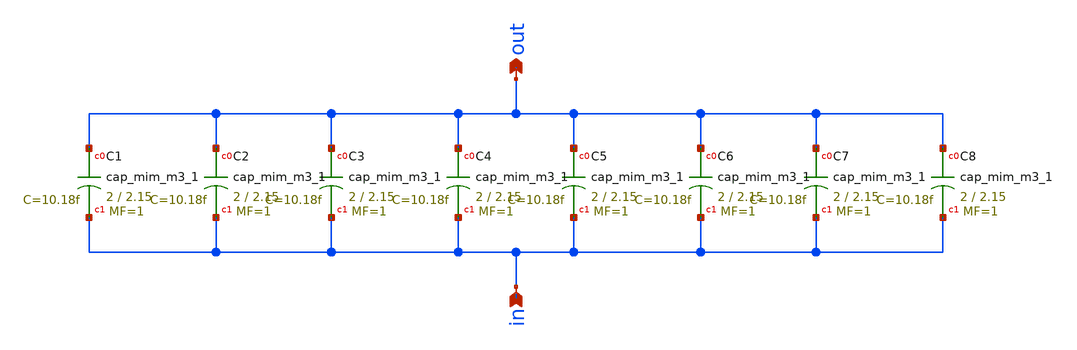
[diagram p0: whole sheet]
** sch_path: xschem/cap8.sch
**.subckt cap8 in out
*.ipin in
*.opin out
XC1 out in sky130_fd_pr__cap_mim_m3_1 W=2 L=2.15 MF=1 m=1
XC2 out in sky130_fd_pr__cap_mim_m3_1 W=2 L=2.15 MF=1 m=1
XC3 out in sky130_fd_pr__cap_mim_m3_1 W=2 L=2.15 MF=1 m=1
XC4 out in sky130_fd_pr__cap_mim_m3_1 W=2 L=2.15 MF=1 m=1
XC5 out in sky130_fd_pr__cap_mim_m3_1 W=2 L=2.15 MF=1 m=1
XC6 out in sky130_fd_pr__cap_mim_m3_1 W=2 L=2.15 MF=1 m=1
XC7 out in sky130_fd_pr__cap_mim_m3_1 W=2 L=2.15 MF=1 m=1
XC8 out in sky130_fd_pr__cap_mim_m3_1 W=2 L=2.15 MF=1 m=1
**.ends
.end
